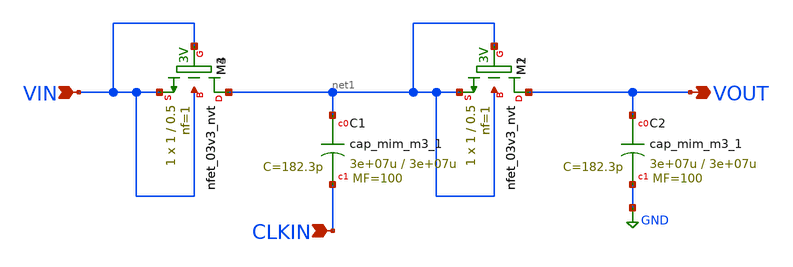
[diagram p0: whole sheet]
** sch_path: xschem/charge_pump/chargepump.sch
**.subckt chargepump VIN CLKIN VOUT
*.ipin VIN
*.ipin CLKIN
*.opin VOUT
XM2 VOUT net1 net1 net1 sky130_fd_pr__nfet_03v3_nvt L=0.5 W=1 nf=1 ad='int((nf+1)/2) * W/nf * 0.29' as='int((nf+2)/2) * W/nf * 0.29'
+ pd='2*int((nf+1)/2) * (W/nf + 0.29)' ps='2*int((nf+2)/2) * (W/nf + 0.29)' nrd='0.29 / W' nrs='0.29 / W'
+ sa=0 sb=0 sd=0 mult=1 m=1
XM1 VOUT net1 net1 net1 sky130_fd_pr__nfet_03v3_nvt L=0.5 W=1 nf=1 ad='int((nf+1)/2) * W/nf * 0.29' as='int((nf+2)/2) * W/nf * 0.29'
+ pd='2*int((nf+1)/2) * (W/nf + 0.29)' ps='2*int((nf+2)/2) * (W/nf + 0.29)' nrd='0.29 / W' nrs='0.29 / W'
+ sa=0 sb=0 sd=0 mult=1 m=1
XM3 net1 VIN VIN VIN sky130_fd_pr__nfet_03v3_nvt L=0.5 W=1 nf=1 ad='int((nf+1)/2) * W/nf * 0.29' as='int((nf+2)/2) * W/nf * 0.29'
+ pd='2*int((nf+1)/2) * (W/nf + 0.29)' ps='2*int((nf+2)/2) * (W/nf + 0.29)' nrd='0.29 / W' nrs='0.29 / W'
+ sa=0 sb=0 sd=0 mult=1 m=1
XM4 net1 VIN VIN VIN sky130_fd_pr__nfet_03v3_nvt L=0.5 W=1 nf=1 ad='int((nf+1)/2) * W/nf * 0.29' as='int((nf+2)/2) * W/nf * 0.29'
+ pd='2*int((nf+1)/2) * (W/nf + 0.29)' ps='2*int((nf+2)/2) * (W/nf + 0.29)' nrd='0.29 / W' nrs='0.29 / W'
+ sa=0 sb=0 sd=0 mult=1 m=1
XC1 net1 CLKIN sky130_fd_pr__cap_mim_m3_1 W=3e+07u L=3e+07u MF=100 m=100
XC2 VOUT GND sky130_fd_pr__cap_mim_m3_1 W=3e+07u L=3e+07u MF=100 m=100
**.ends
.GLOBAL GND
.end
